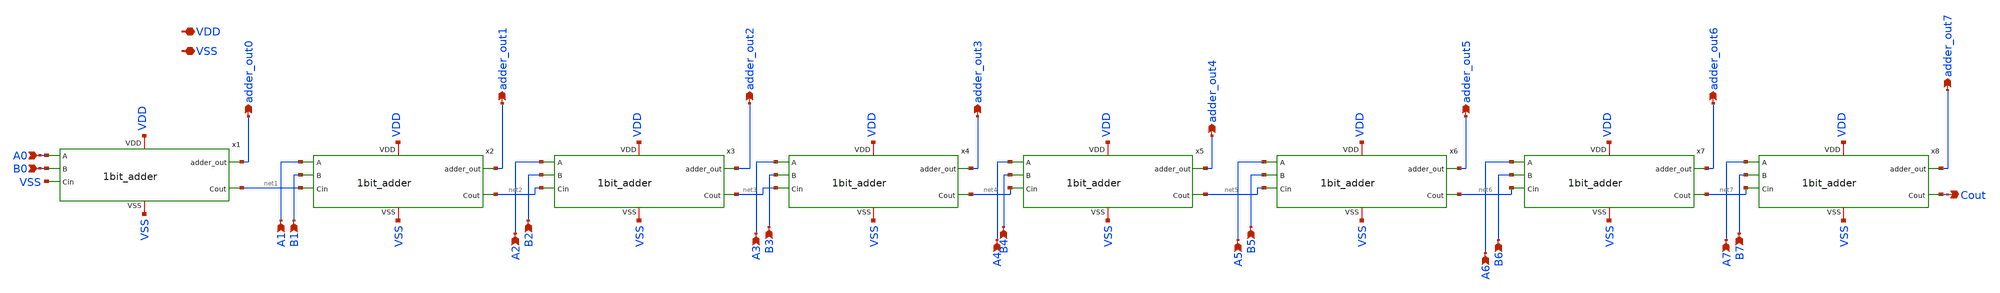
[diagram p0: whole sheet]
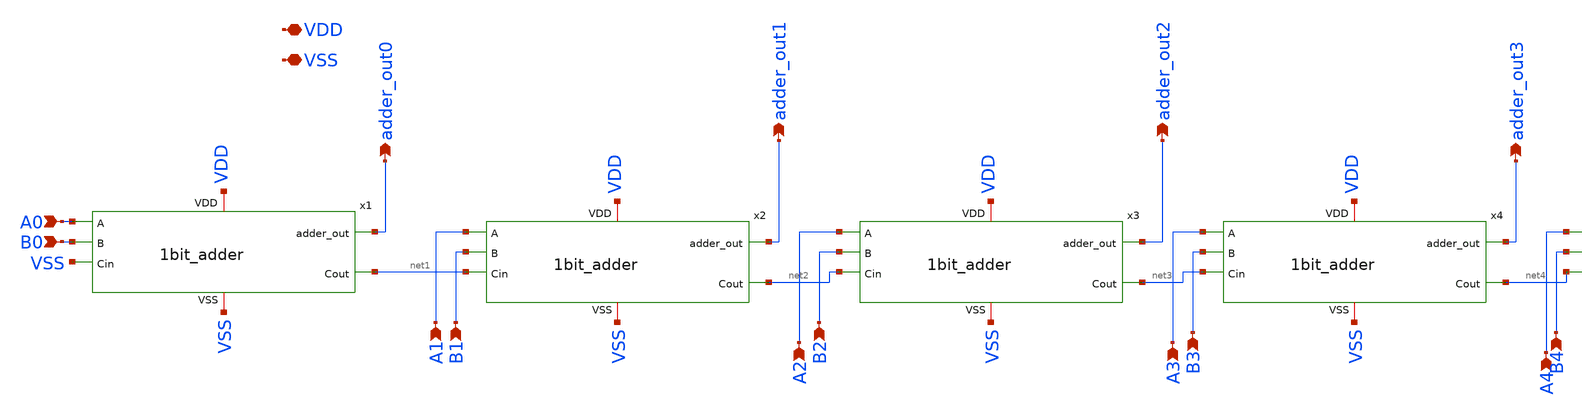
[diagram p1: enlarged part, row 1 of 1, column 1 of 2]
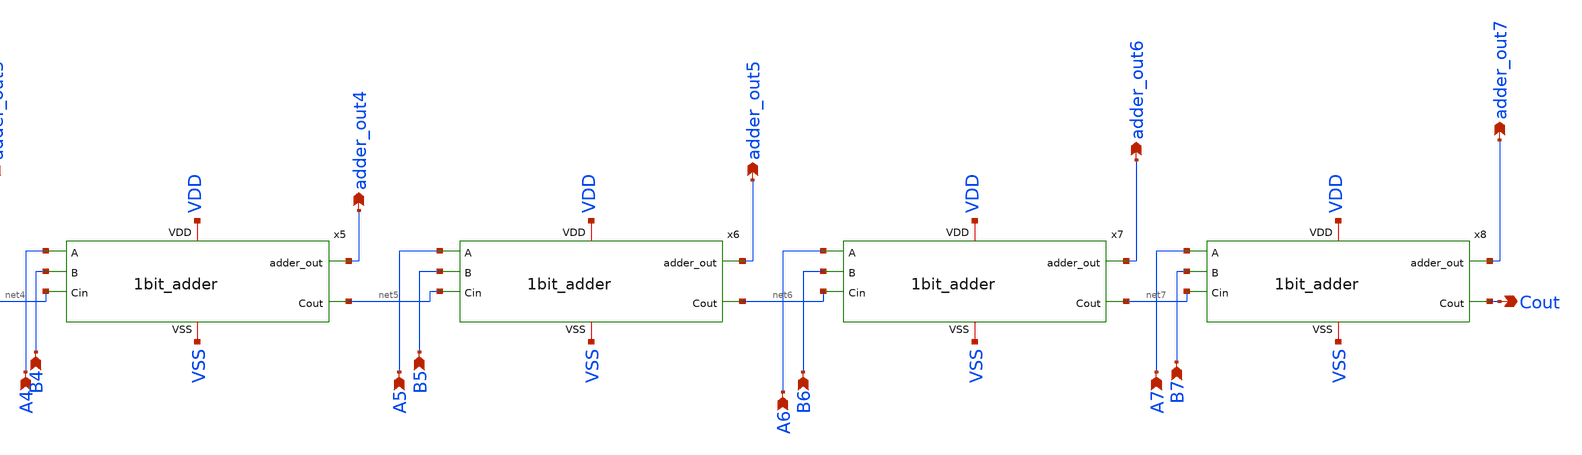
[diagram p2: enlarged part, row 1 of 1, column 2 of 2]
** sch_path: 8bit_adder.sch
**.subckt 8bit_adder VDD VSS A0 B0 adder_out0 A1 B1 adder_out1 A2 B2 adder_out2 A3 B3 adder_out3 A4
*+ B4 adder_out4 A5 B5 A6 B6 adder_out5 A7 B7 adder_out6 adder_out7 Cout
*.iopin VDD
*.iopin VSS
*.ipin A0
*.ipin B0
*.opin adder_out0
*.ipin A1
*.ipin B1
*.opin adder_out1
*.ipin A2
*.ipin B2
*.opin adder_out2
*.ipin A3
*.ipin B3
*.opin adder_out3
*.ipin A4
*.ipin B4
*.opin adder_out4
*.ipin A5
*.ipin B5
*.ipin A6
*.ipin B6
*.opin adder_out5
*.ipin A7
*.ipin B7
*.opin adder_out6
*.opin adder_out7
*.opin Cout
x1 VDD VSS A0 adder_out0 B0 net1 VSS 1bit_adder
x2 VDD VSS A1 adder_out1 B1 net2 net1 1bit_adder
x3 VDD VSS A2 adder_out2 B2 net3 net2 1bit_adder
x4 VDD VSS A3 adder_out3 B3 net4 net3 1bit_adder
x5 VDD VSS A4 adder_out4 B4 net5 net4 1bit_adder
x6 VDD VSS A5 adder_out5 B5 net6 net5 1bit_adder
x7 VDD VSS A6 adder_out6 B6 net7 net6 1bit_adder
x8 VDD VSS A7 adder_out7 B7 Cout net7 1bit_adder
**.ends
.end
